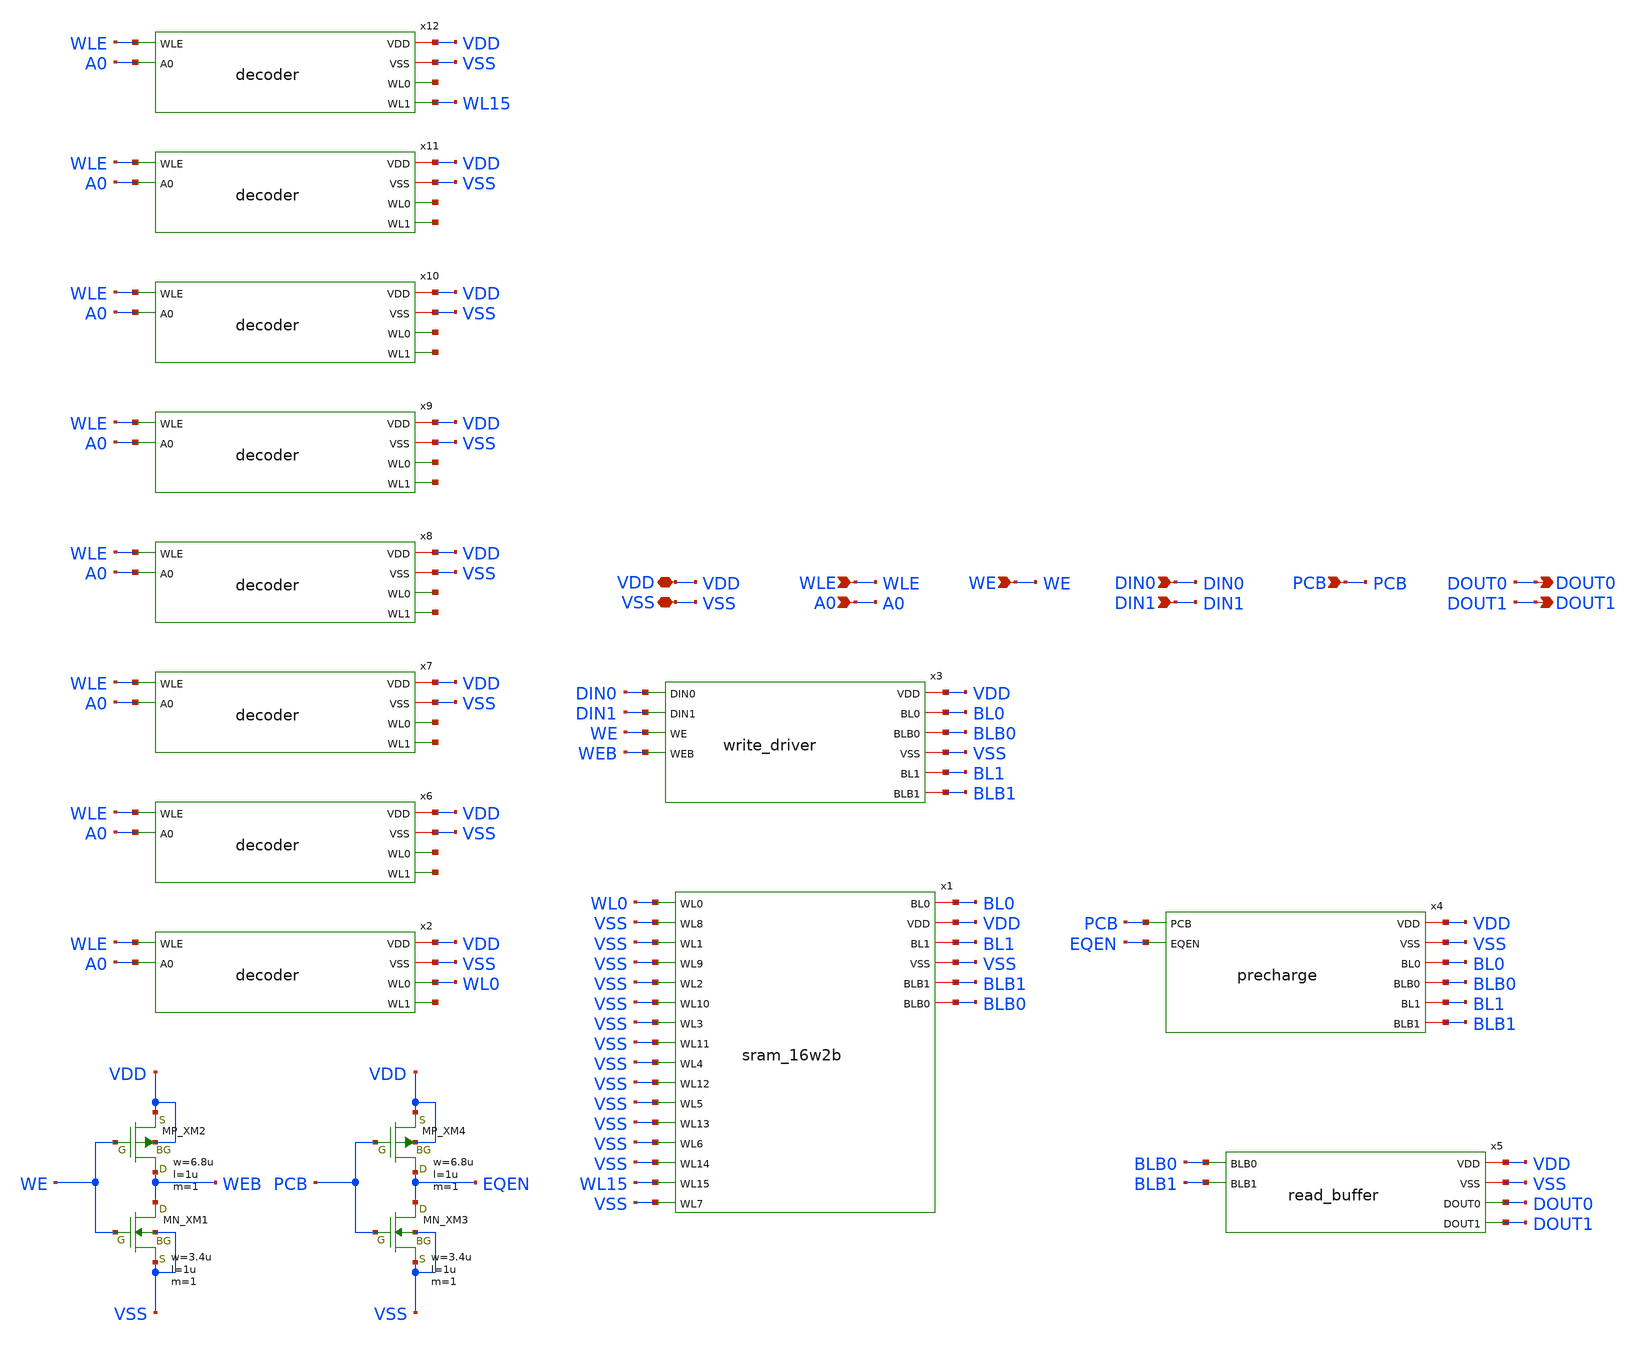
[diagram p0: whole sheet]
** sch_path: sram/sram_16w2b_top.sch
**.subckt sram_16w2b_top VDD WLE DOUT0 VSS A0 WE DIN0 DIN1 PCB DOUT1
*.iopin VDD
*.ipin WLE
*.opin DOUT0
*.iopin VSS
*.ipin A0
*.ipin WE
*.ipin DIN0
*.ipin DIN1
*.ipin PCB
*.opin DOUT1
x2 VDD VSS WL0 WLE A0 net1 decoder
x3 DIN0 VDD BL0 BLB0 VSS DIN1 BL1 WE BLB1 WEB write_driver
x4 VDD VSS PCB EQEN BL0 BLB0 BL1 BLB1 precharge
x5 VDD VSS BLB0 BLB1 DOUT0 DOUT1 read_buffer
XXM1 WEB WE VSS VSS NMOS w=3.4u l=1u nrd=0 nrs=0 m=1
XXM2 WEB WE VDD VDD PMOS w=6.8u l=1u nrd=0 nrs=0 m=1
XXM3 EQEN PCB VSS VSS NMOS w=3.4u l=1u nrd=0 nrs=0 m=1
XXM4 EQEN PCB VDD VDD PMOS w=6.8u l=1u nrd=0 nrs=0 m=1
x1 BL0 VDD WL0 VSS BL1 VSS VSS BLB1 VSS BLB0 VSS VSS VSS VSS VSS VSS VSS VSS VSS VSS WL15 VSS
+ sram_16w2b
x6 VDD VSS net2 WLE A0 net3 decoder
x7 VDD VSS net4 WLE A0 net5 decoder
x8 VDD VSS net6 WLE A0 net7 decoder
x9 VDD VSS net8 WLE A0 net9 decoder
x10 VDD VSS net10 WLE A0 net11 decoder
x11 VDD VSS net12 WLE A0 net13 decoder
x12 VDD VSS net14 WLE A0 WL15 decoder
**.ends
.end
